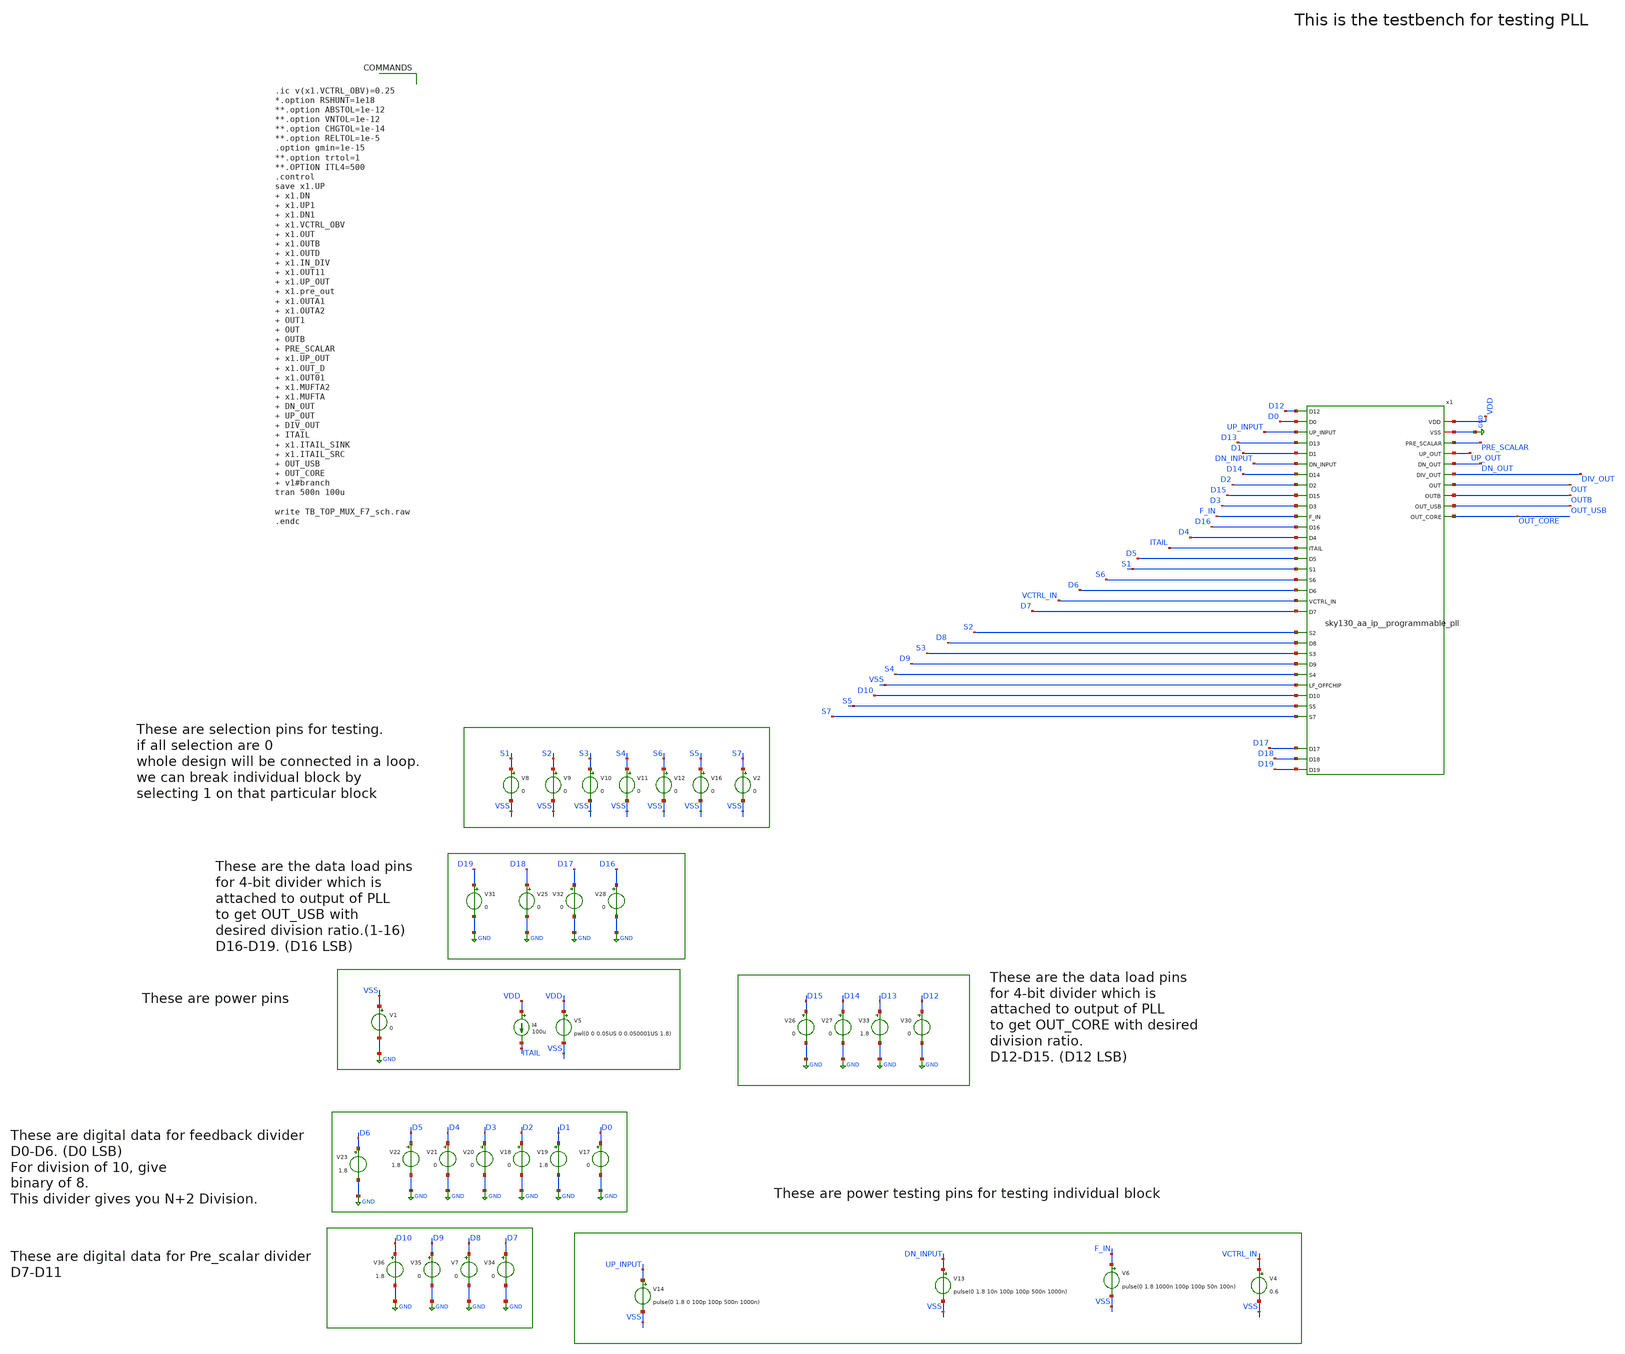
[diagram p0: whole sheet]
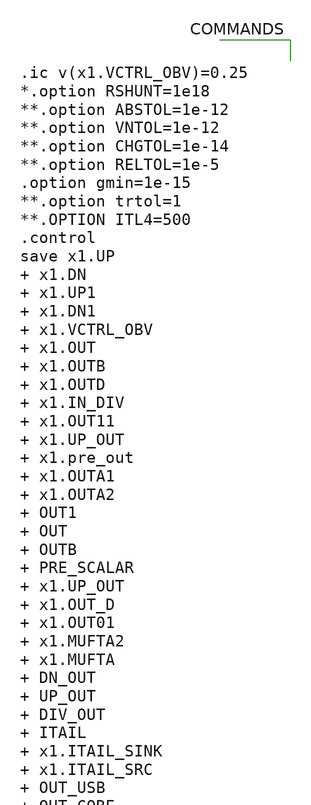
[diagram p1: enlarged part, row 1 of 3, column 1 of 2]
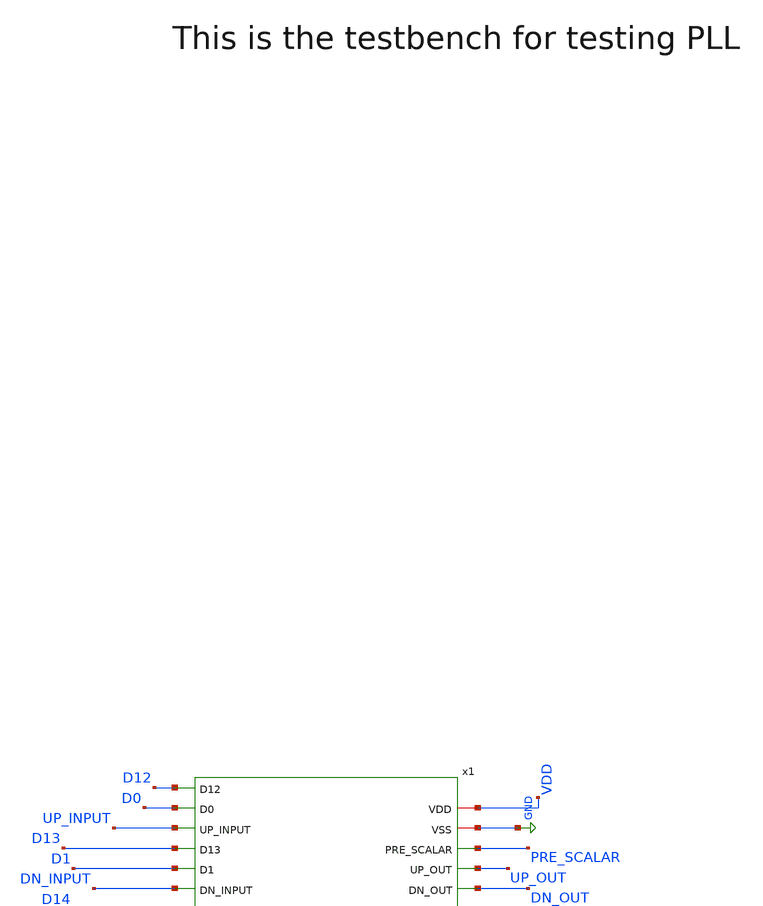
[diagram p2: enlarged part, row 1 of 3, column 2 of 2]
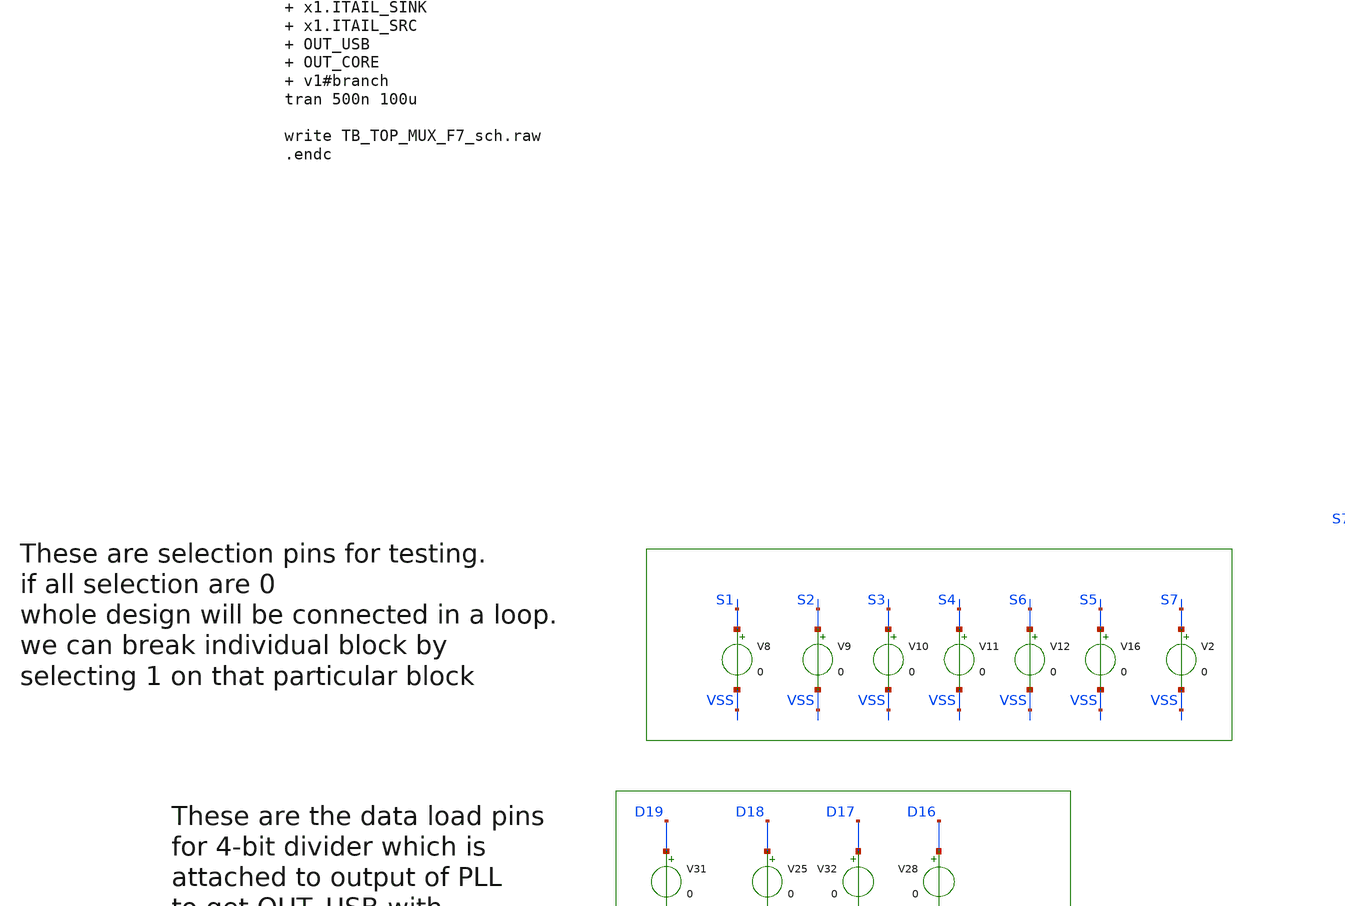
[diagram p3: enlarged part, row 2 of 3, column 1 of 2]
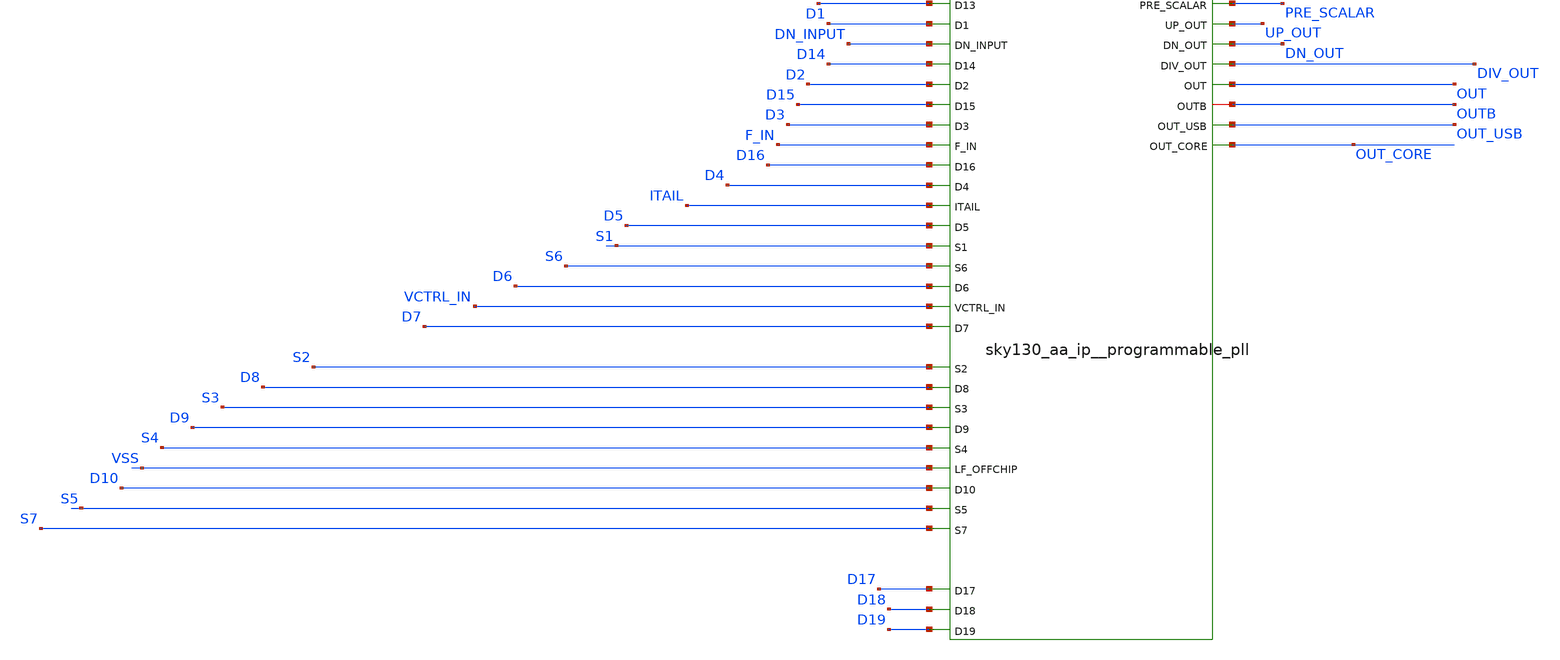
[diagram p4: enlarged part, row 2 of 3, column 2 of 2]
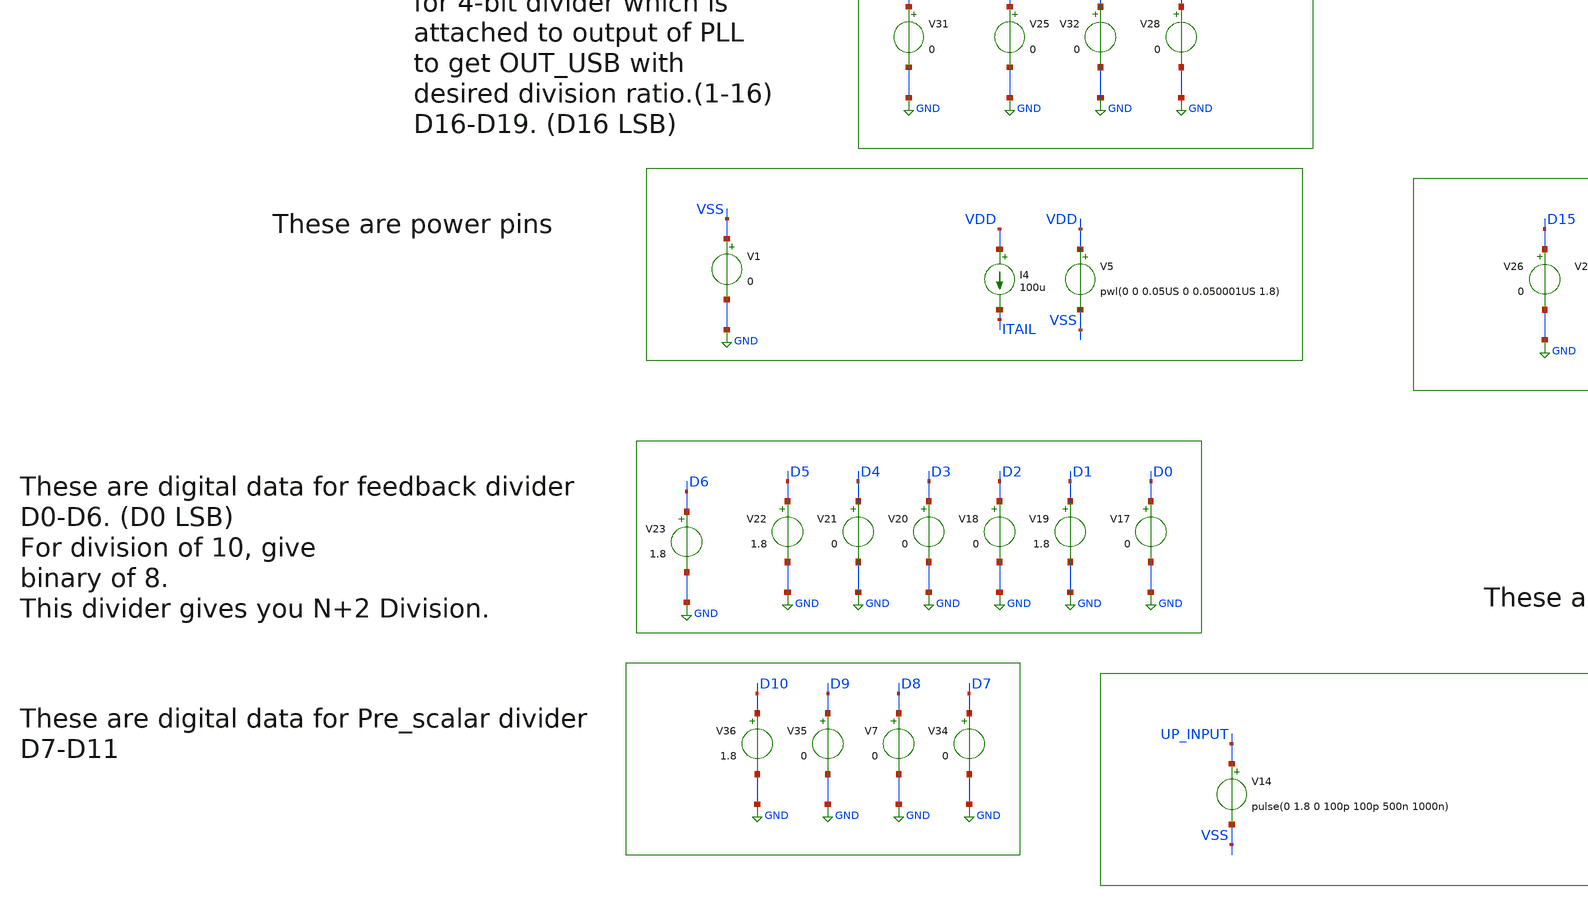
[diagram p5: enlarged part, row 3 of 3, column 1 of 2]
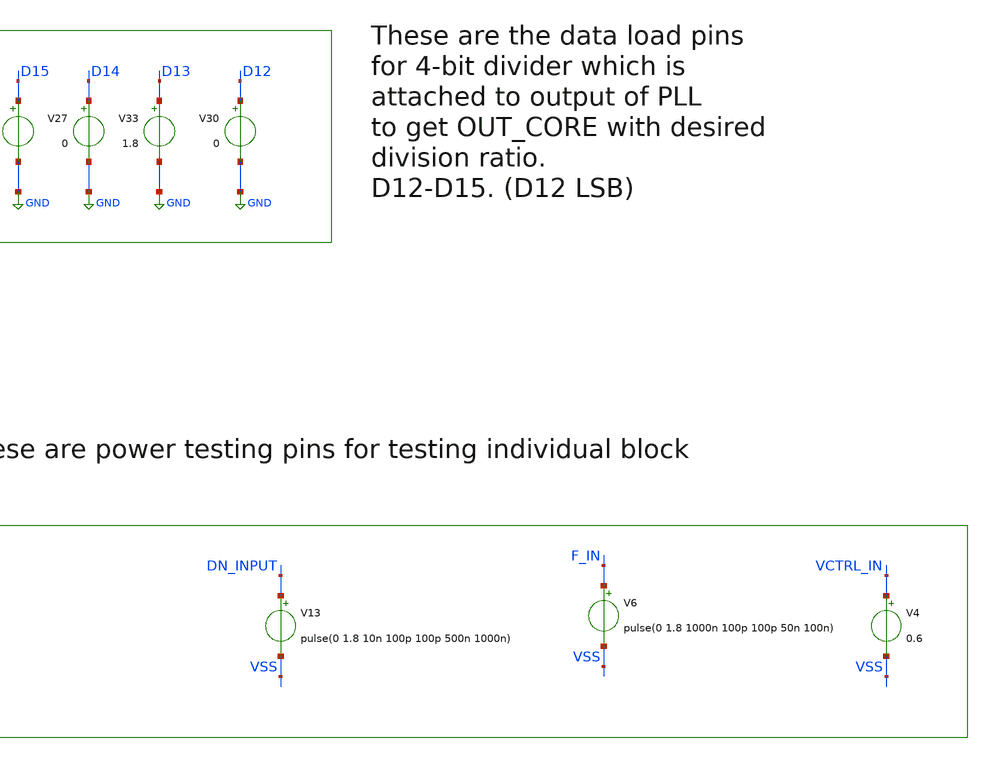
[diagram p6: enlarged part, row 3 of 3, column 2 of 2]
** sch_path: xschem/PLL_top_tran_tb.sch
**.subckt PLL_top_tran_tb
V1 VSS GND 0
V4 VCTRL_IN VSS 0.6
V6 F_IN VSS pulse(0 1.8 1000n 100p 100p 50n 100n)
I4 VDD ITAIL 100u
V8 S1 VSS 0
V9 S2 VSS 0
V10 S3 VSS 0
V11 S4 VSS 0
V12 S6 VSS 0
V13 DN_INPUT VSS pulse(0 1.8 10n 100p 100p 500n 1000n)
V14 UP_INPUT VSS pulse(0 1.8 0 100p 100p 500n 1000n)
V16 S5 VSS 0
V17 D0 GND 0
V2 S7 VSS 0
V5 VDD VSS pwl(0 0 0.05US 0 0.050001US 1.8)
V35 D9 GND 0
V20 D3 GND 0
V22 D5 GND 1.8
V36 D10 GND 1.8
V7 D8 GND 0
V34 D7 GND 0
V21 D4 GND 0
V23 D6 GND 1.8
V25 D18 GND 0
V26 D15 GND 0
V31 D19 GND 0
V28 D16 GND 0
V27 D14 GND 0
V30 D12 GND 0
V32 D17 GND 0
V18 D2 GND 0
V19 D1 GND 1.8
V33 D13 GND 1.8
x1 D12 D0 VDD UP_INPUT D13 D1 DN_INPUT GND D14 D2 PRE_SCALAR UP_OUT D15 D3 F_IN DN_OUT D16 D4 ITAIL
+ DIV_OUT D5 S1 S6 D6 VCTRL_IN D7 S2 D8 S3 OUT D9 OUTB S4 VSS D10 S5 S7 OUT_USB D17 OUT_CORE D18 D19
+ sky130_aa_ip__programmable_pll
**** begin user architecture code


.ic v(x1.VCTRL_OBV)=0.25
*.option RSHUNT=1e18
**.option ABSTOL=1e-12
**.option VNTOL=1e-12
**.option CHGTOL=1e-14
**.option RELTOL=1e-5
.option gmin=1e-15
**.option trtol=1
**.OPTION ITL4=500
.control
save x1.UP  x1.DN  x1.UP1  x1.DN1  x1.VCTRL_OBV  x1.OUT  x1.OUTB  x1.OUTD  x1.IN_DIV  x1.OUT11
+  x1.UP_OUT  x1.pre_out  x1.OUTA1  x1.OUTA2  OUT1  OUT  OUTB  PRE_SCALAR  x1.UP_OUT  x1.OUT_D  x1.OUT01
+  x1.MUFTA2  x1.MUFTA  DN_OUT  UP_OUT  DIV_OUT  ITAIL  x1.ITAIL_SINK  x1.ITAIL_SRC  OUT_USB  OUT_CORE
+  v1#branch
tran 500n 100u

write TB_TOP_MUX_F7_sch.raw
.endc



** opencircuitdesign pdks install
*.lib $::SKYWATER_MODELS/sky130.lib.spice tt
*cannot simulate using combined models due to small finger width of m.x1.x8.xm10
*temporarily switcing to discrete models
.lib $::SKYWATER_MODELS/../ngspice/sky130.lib.spice tt


**** end user architecture code
**.ends
.GLOBAL GND
.end
